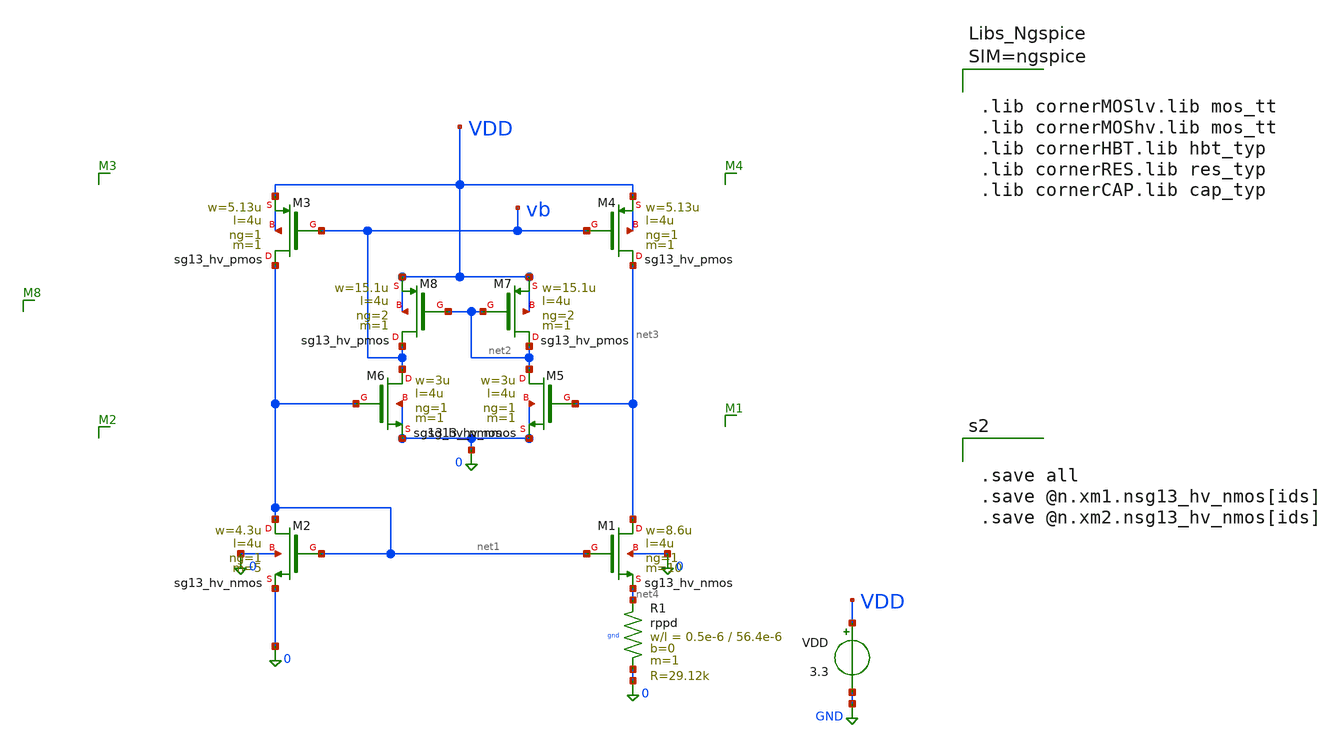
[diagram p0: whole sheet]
** sch_path: design/BMR2U.sch
**.subckt BMR2U
VDD VDD GND 3.3
XM1 net3 net1 net4 0 sg13_hv_nmos w=8.6u l=4u ng=1 m=10 mm_ok=1
XM2 net1 net1 0 0 sg13_hv_nmos w=4.3u l=4u ng=1 m=5 mm_ok=1
XM3 net1 vb VDD VDD sg13_hv_pmos w=5.13u l=4u ng=1 m=1 mm_ok=1
XM4 net3 vb VDD VDD sg13_hv_pmos w=5.13u l=4u ng=1 m=1 mm_ok=1
XM5 net2 net3 0 0 sg13_hv_nmos w=3u l=4u ng=1 m=1 mm_ok=1
XM6 vb net1 0 0 sg13_hv_nmos w=3u l=4u ng=1 m=1 mm_ok=1
XM7 net2 net2 VDD VDD sg13_hv_pmos w=15.1u l=4u ng=2 m=1 mm_ok=1
XM8 vb net2 VDD VDD sg13_hv_pmos w=15.1u l=4u ng=2 m=1 mm_ok=1
XR1 net4 0 gnd rppd w=0.5e-6 l=56.4e-6 m=1 b=0 mm_ok=1
**** begin user architecture code


.include BMR2U.save
.control
* ---------- Operating point ----------
op
write BMR2U.raw
let id1_uA = abs(@n.xm1.nsg13_hv_nmos[ids])*1e6
let id2_uA = abs(@n.xm2.nsg13_hv_nmos[ids])*1e6
let gm1_uS = @n.xm1.nsg13_hv_nmos[gm]*1e6
let gm2_uS = @n.xm2.nsg13_hv_nmos[gm]*1e6
let vgs_M1 = v(net1)-v(net4)
let vgs_M2 = v(net1)
let vdsat_M1 = @n.xm1.nsg13_hv_nmos[vdss]
let vdsat_M2 = @n.xm2.nsg13_hv_nmos[vdss]
let vdsat_M3 = abs(@n.xm3.nsg13_hv_pmos[vdss])
let vdsat_M4 = abs(@n.xm4.nsg13_hv_pmos[vdss])
print v(vb) vgs_M1 vgs_M2
print id1_uA id2_uA gm1_uS gm2_uS
print vdsat_M1 vdsat_M2 vdsat_M3 vdsat_M4

* ---------- Line regulation (VDD sweep) ----------
dc vdd 0 4 10m
let id1_uA = @n.xm1.nsg13_hv_nmos[ids]*1e6
let id2_uA = @n.xm2.nsg13_hv_nmos[ids]*1e6
plot id1_uA id2_uA
meas dc id1_3p0 find id1_uA at=3.0
meas dc id1_3p6 find id1_uA at=3.6
let line_reg = (id1_3p6-id1_3p0)/id1_3p0/0.6*100
echo Line regulation [%/V] = $&line_reg

* ---------- Temperature coefficient (VDD = 3.3 V) ----------
dc temp -40 125 1
let id1_uA = abs(@n.xm1.nsg13_hv_nmos[ids])*1e6
let id2_uA = abs(@n.xm2.nsg13_hv_nmos[ids])*1e6
plot id1_uA id2_uA
meas dc id1_max max id1_uA
meas dc id1_min min id1_uA
meas dc id1_27 find id1_uA at=27
let tc = (id1_max-id1_min)/id1_27/165*1e6
echo TC [ppm/C] = $&tc
.endc




.save all
.save @n.xm1.nsg13_hv_nmos[ids]
.save @n.xm2.nsg13_hv_nmos[ids]






.lib cornerMOSlv.lib mos_tt
.lib cornerMOShv.lib mos_tt
.lib cornerHBT.lib hbt_typ
.lib cornerRES.lib res_typ
.lib cornerCAP.lib cap_typ



**** end user architecture code
**.ends
.GLOBAL GND
.end
